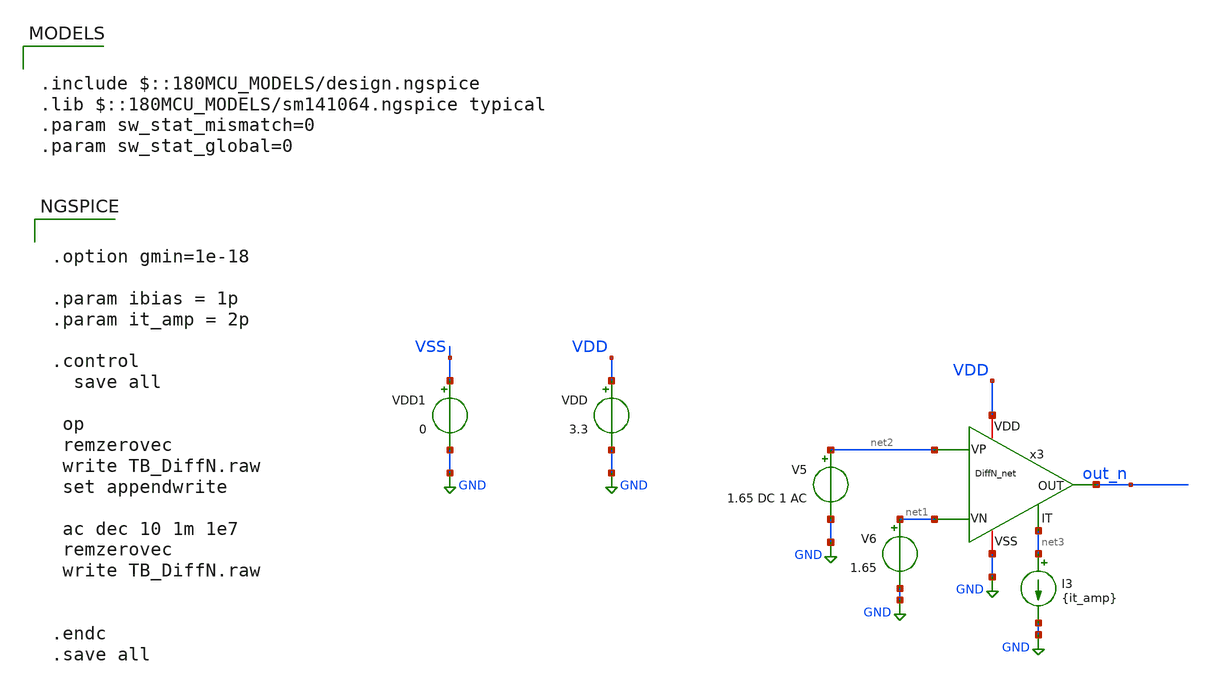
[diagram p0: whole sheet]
** sch_path: TIA_Filter/PseudoResistor/TB_DiffN.sch
**.subckt TB_DiffN
VDD VDD GND 3.3
x3 net1 net2 out_n net3 VDD GND DiffN_net
V5 net2 GND 1.65 DC 1 AC
V6 net1 GND 1.65
I3 net3 GND {it_amp}
VDD1 VSS GND 0
**** begin user architecture code

.include $::180MCU_MODELS/design.ngspice
.lib $::180MCU_MODELS/sm141064.ngspice typical
.param sw_stat_mismatch=0
.param sw_stat_global=0



.option gmin=1e-18

.param ibias = 1p
.param it_amp = 2p

.control
  save all

 op
 remzerovec
 write TB_DiffN.raw
 set appendwrite

 ac dec 10 1m 1e7
 remzerovec
 write TB_DiffN.raw


.endc
.save all


**** end user architecture code
**.ends
.GLOBAL GND
.end
